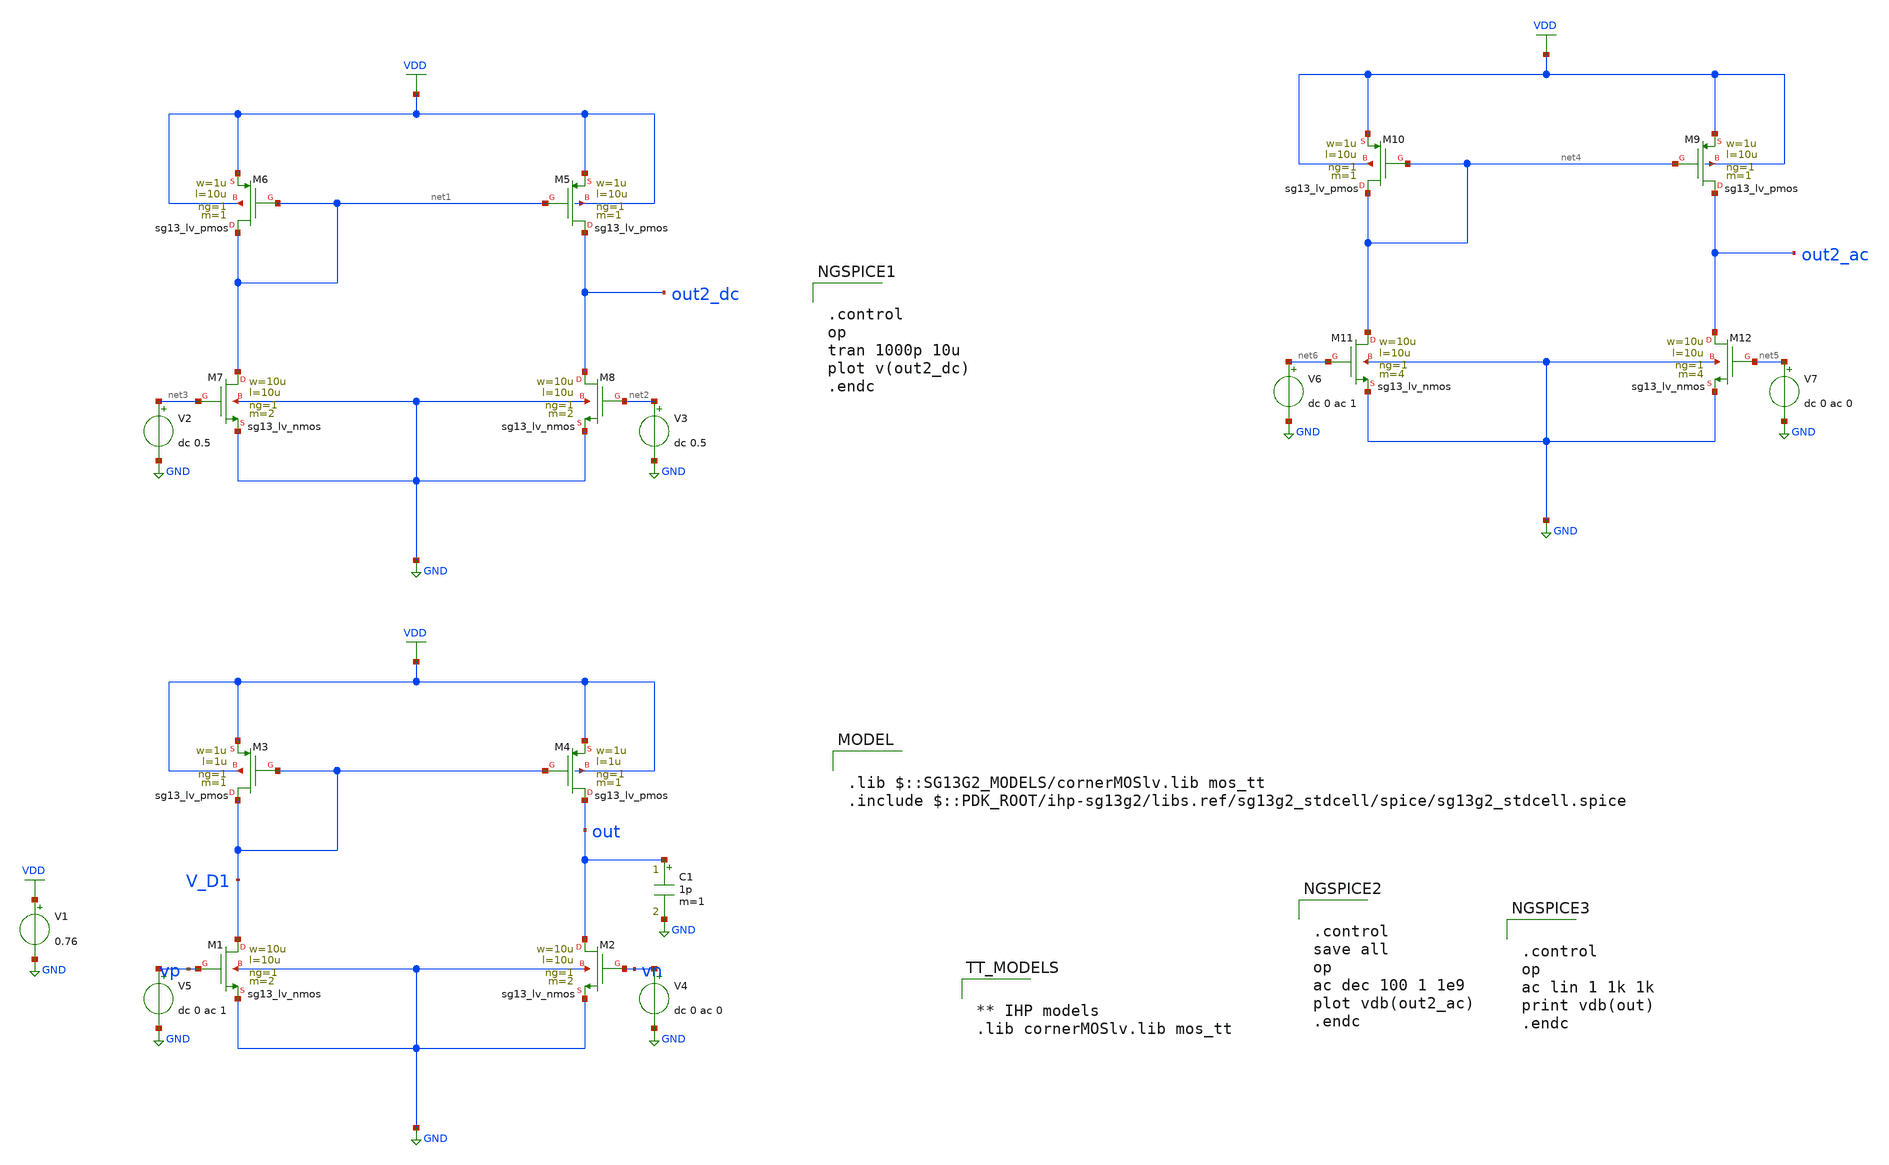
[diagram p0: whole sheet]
** sch_path: SSDOR_1.2V_v2/components/Ib_4u/Ib_4u_opamp/tb_Ib_4u_opamp.sch

.lib $::SG13G2_MODELS/cornerMOSlv.lib mos_tt
.include $::PDK_ROOT/ihp-sg13g2/libs.ref/sg13g2_stdcell/spice/sg13g2_stdcell.spice

**.subckt tb_Ib_4u_opamp
V1 VDD GND 0.76
XM4 out V_D1 VDD VDD sg13_lv_pmos w=1u l=1u ng=1 m=1 mm_ok=1
XM3 V_D1 V_D1 VDD VDD sg13_lv_pmos w=1u l=1u ng=1 m=1 mm_ok=1
XM1 V_D1 vp GND GND sg13_lv_nmos w=10u l=10u ng=1 m=2 mm_ok=1
XM2 out vn GND GND sg13_lv_nmos w=10u l=10u ng=1 m=2 mm_ok=1
C1 out GND 1p m=1
V4 vn GND dc 0 ac 0
V5 vp GND dc 0 ac 1
XM5 out2_dc net1 VDD VDD sg13_lv_pmos w=1u l=10u ng=1 m=1 mm_ok=1
XM6 net1 net1 VDD VDD sg13_lv_pmos w=1u l=10u ng=1 m=1 mm_ok=1
XM7 net1 net3 GND GND sg13_lv_nmos w=10u l=10u ng=1 m=2 mm_ok=1
XM8 out2_dc net2 GND GND sg13_lv_nmos w=10u l=10u ng=1 m=2 mm_ok=1
V2 net3 GND dc 0.5
V3 net2 GND dc 0.5
XM9 out2_ac net4 VDD VDD sg13_lv_pmos w=1u l=10u ng=1 m=1 mm_ok=1
XM10 net4 net4 VDD VDD sg13_lv_pmos w=1u l=10u ng=1 m=1 mm_ok=1
XM11 net4 net6 GND GND sg13_lv_nmos w=10u l=10u ng=1 m=4 mm_ok=1
XM12 out2_ac net5 GND GND sg13_lv_nmos w=10u l=10u ng=1 m=4 mm_ok=1
V6 net6 GND dc 0 ac 1
V7 net5 GND dc 0 ac 0
**** begin user architecture code


** IHP models
.lib cornerMOSlv.lib mos_tt




.control
op
tran 1000p 10u
plot v(out2_dc)
.endc





.control
save all
op
ac dec 100 1 1e9
plot vdb(out2_ac)
.endc






.control
op
ac lin 1 1k 1k
print vdb(out)
.endc


**** end user architecture code
**.ends
.GLOBAL VDD
.GLOBAL GND
.end
